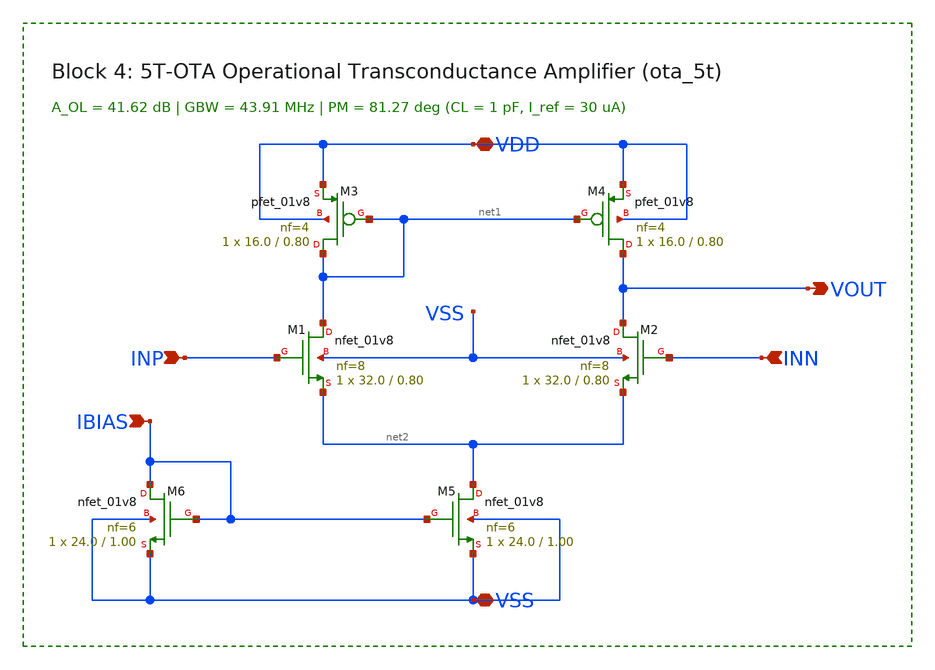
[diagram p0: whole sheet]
** sch_path: sky130-sc-lpf/xschem/ota_5t.sch
**.subckt ota_5t VDD VOUT INP INN IBIAS VSS
*.iopin VDD
*.opin VOUT
*.ipin INP
*.ipin INN
*.ipin IBIAS
*.iopin VSS
XM3 net1 net1 VDD VDD sky130_fd_pr__pfet_01v8 L=0.80 W=16.0 nf=4 ad='int((nf+1)/2) * W/nf * 0.29' as='int((nf+2)/2) * W/nf * 0.29'
+ pd='2*int((nf+1)/2) * (W/nf + 0.29)' ps='2*int((nf+2)/2) * (W/nf + 0.29)' nrd='0.29 / W' nrs='0.29 / W'
+ sa=0 sb=0 sd=0 mult=1 m=1
XM4 VOUT net1 VDD VDD sky130_fd_pr__pfet_01v8 L=0.80 W=16.0 nf=4 ad='int((nf+1)/2) * W/nf * 0.29' as='int((nf+2)/2) * W/nf * 0.29'
+ pd='2*int((nf+1)/2) * (W/nf + 0.29)' ps='2*int((nf+2)/2) * (W/nf + 0.29)' nrd='0.29 / W' nrs='0.29 / W'
+ sa=0 sb=0 sd=0 mult=1 m=1
XM1 net1 INP net2 VSS sky130_fd_pr__nfet_01v8 L=0.80 W=32.0 nf=8 ad='int((8 + 1)/2) * 32.0 / 8 * 0.29'
+ as='int((8 + 2)/2) * 32.0 / 8 * 0.29' pd='2*int((8 + 1)/2) * (32.0 / 8 + 0.29)' ps='2*int((8 + 2)/2) * (32.0 / 8 + 0.29)'
+ nrd='0.29 / 32.0 ' nrs='0.29 / 32.0 ' sa=0 sb=0 sd=0 mult=1 m=1
XM2 VOUT INN net2 VSS sky130_fd_pr__nfet_01v8 L=0.80 W=32.0 nf=8 ad='int((8 + 1)/2) * 32.0 / 8 * 0.29'
+ as='int((8 + 2)/2) * 32.0 / 8 * 0.29' pd='2*int((8 + 1)/2) * (32.0 / 8 + 0.29)' ps='2*int((8 + 2)/2) * (32.0 / 8 + 0.29)'
+ nrd='0.29 / 32.0 ' nrs='0.29 / 32.0 ' sa=0 sb=0 sd=0 mult=1 m=1
XM5 net2 IBIAS VSS VSS sky130_fd_pr__nfet_01v8 L=1.00 W=24.0 nf=6 ad='int((6 + 1)/2) * 24.0 / 6 * 0.29'
+ as='int((6 + 2)/2) * 24.0 / 6 * 0.29' pd='2*int((6 + 1)/2) * (24.0 / 6 + 0.29)' ps='2*int((6 + 2)/2) * (24.0 / 6 + 0.29)'
+ nrd='0.29 / 24.0 ' nrs='0.29 / 24.0 ' sa=0 sb=0 sd=0 mult=1 m=1
XM6 IBIAS IBIAS VSS VSS sky130_fd_pr__nfet_01v8 L=1.00 W=24.0 nf=6 ad='int((6 + 1)/2) * 24.0 / 6 * 0.29'
+ as='int((6 + 2)/2) * 24.0 / 6 * 0.29' pd='2*int((6 + 1)/2) * (24.0 / 6 + 0.29)' ps='2*int((6 + 2)/2) * (24.0 / 6 + 0.29)'
+ nrd='0.29 / 24.0 ' nrs='0.29 / 24.0 ' sa=0 sb=0 sd=0 mult=1 m=1
**.ends
.end
